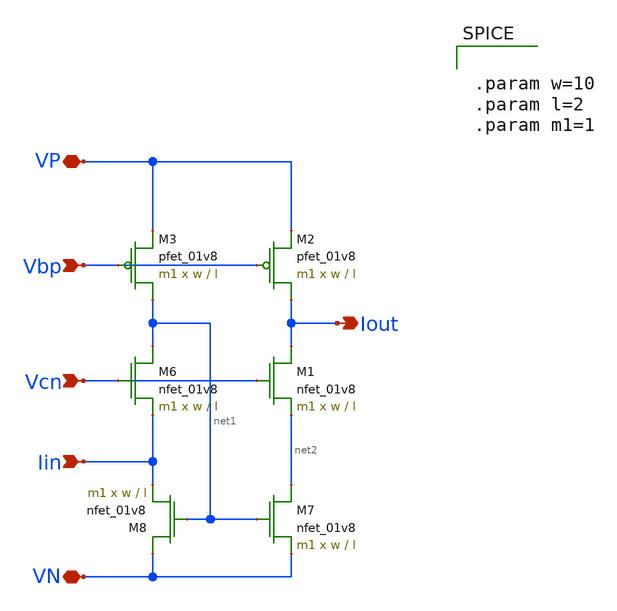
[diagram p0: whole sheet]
** sch_path: schematic/iout_mirror.sch
**.subckt iout_mirror Vbp VN Iin Vcn VP Iout
*.ipin Vbp
*.iopin VN
*.ipin Iin
*.ipin Vcn
*.iopin VP
*.opin Iout
XM3 net1 Vbp VP VDD sky130_fd_pr__pfet_01v8 L=l W=w nf=1 ad='int((nf+1)/2) * W/nf * 0.29' as='int((nf+2)/2) * W/nf * 0.29'
+ pd='2*int((nf+1)/2) * (W/nf + 0.29)' ps='2*int((nf+2)/2) * (W/nf + 0.29)' nrd='0.29 / W' nrs='0.29 / W'
+ sa=0 sb=0 sd=0 mult=m1 m=m1
XM6 net1 Vcn Iin GND sky130_fd_pr__nfet_01v8 L=l W=w nf=1 ad='int((nf+1)/2) * W/nf * 0.29' as='int((nf+2)/2) * W/nf * 0.29'
+ pd='2*int((nf+1)/2) * (W/nf + 0.29)' ps='2*int((nf+2)/2) * (W/nf + 0.29)' nrd='0.29 / W' nrs='0.29 / W'
+ sa=0 sb=0 sd=0 mult=m1 m=m1
XM2 Iout Vbp VP VDD sky130_fd_pr__pfet_01v8 L=l W=w nf=1 ad='int((nf+1)/2) * W/nf * 0.29' as='int((nf+2)/2) * W/nf * 0.29'
+ pd='2*int((nf+1)/2) * (W/nf + 0.29)' ps='2*int((nf+2)/2) * (W/nf + 0.29)' nrd='0.29 / W' nrs='0.29 / W'
+ sa=0 sb=0 sd=0 mult=m1 m=m1
XM1 Iout Vcn net2 GND sky130_fd_pr__nfet_01v8 L=l W=w nf=1 ad='int((nf+1)/2) * W/nf * 0.29' as='int((nf+2)/2) * W/nf * 0.29'
+ pd='2*int((nf+1)/2) * (W/nf + 0.29)' ps='2*int((nf+2)/2) * (W/nf + 0.29)' nrd='0.29 / W' nrs='0.29 / W'
+ sa=0 sb=0 sd=0 mult=m1 m=m1
XM7 net2 net1 VN GND sky130_fd_pr__nfet_01v8 L=l W=w nf=1 ad='int((nf+1)/2) * W/nf * 0.29' as='int((nf+2)/2) * W/nf * 0.29'
+ pd='2*int((nf+1)/2) * (W/nf + 0.29)' ps='2*int((nf+2)/2) * (W/nf + 0.29)' nrd='0.29 / W' nrs='0.29 / W'
+ sa=0 sb=0 sd=0 mult=m1 m=m1
XM8 VN net1 Iin GND sky130_fd_pr__nfet_01v8 L=l W=w nf=1 ad='int((nf+1)/2) * W/nf * 0.29' as='int((nf+2)/2) * W/nf * 0.29'
+ pd='2*int((nf+1)/2) * (W/nf + 0.29)' ps='2*int((nf+2)/2) * (W/nf + 0.29)' nrd='0.29 / W' nrs='0.29 / W'
+ sa=0 sb=0 sd=0 mult=m1 m=m1
**** begin user architecture code


.param w=10
.param l=2
.param m1=1


**** end user architecture code
**.ends
.end
